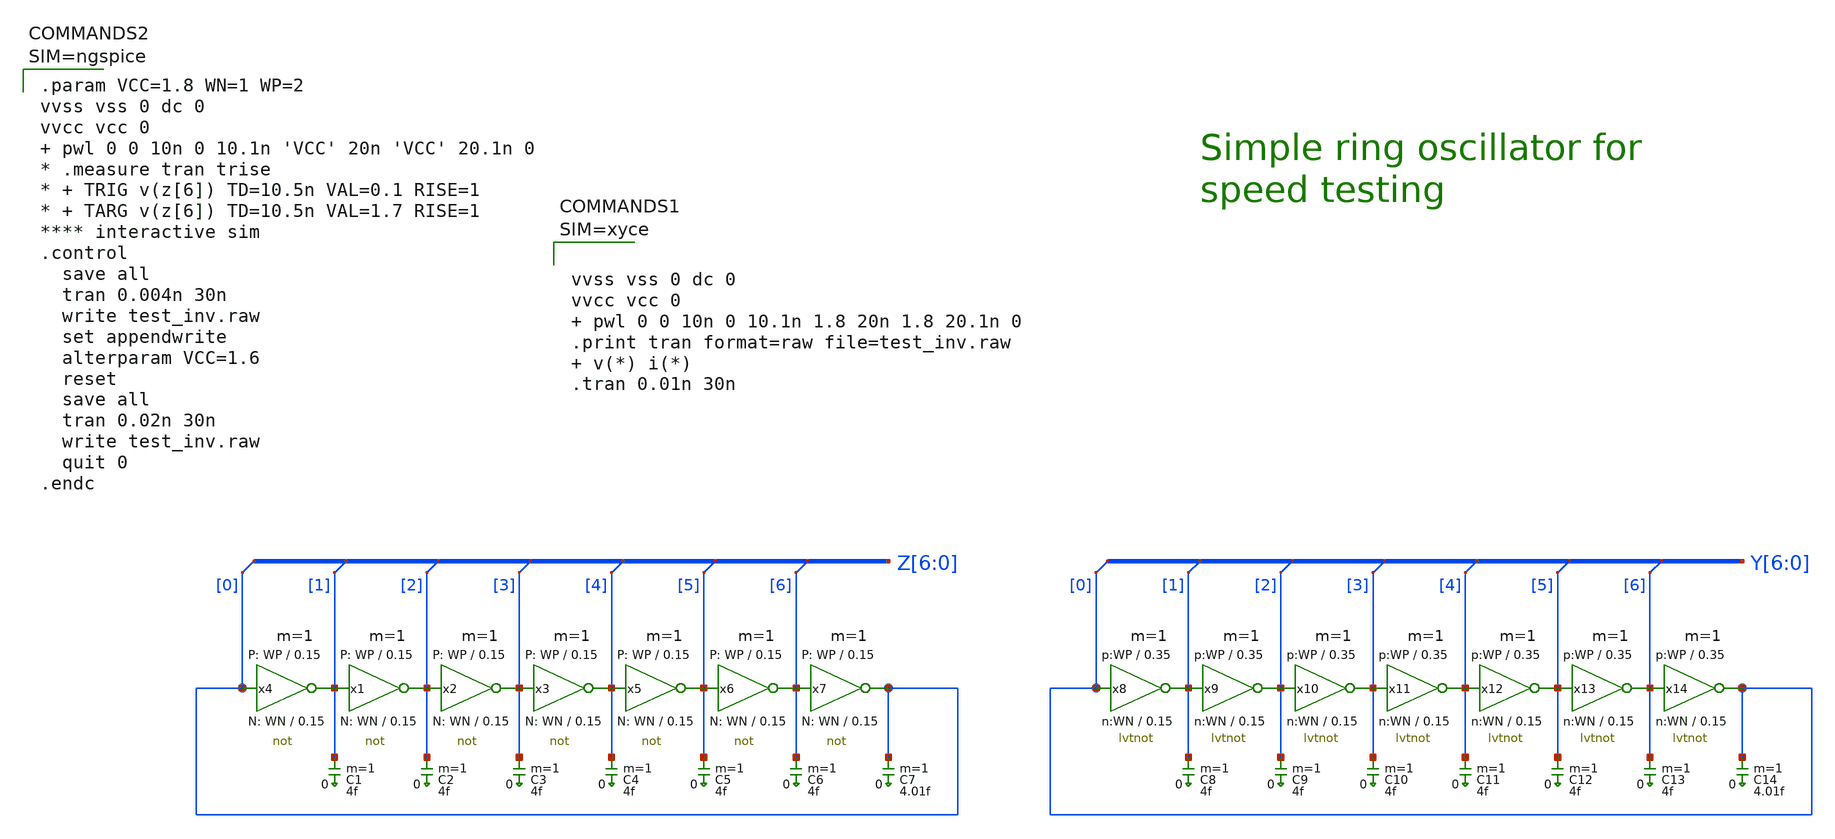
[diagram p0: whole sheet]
** sch_path: sky130A/xschem_libs/sky130_tests/test_inv/schematic/test_inv.sch
* Copyright 2021 Stefan Frederik Schippers
* Licensed under the Apache License, Version 2.0 (the "License");
* you may not use this file except in compliance with the License.
* You may obtain a copy of the License at
* https://www.apache.org/licenses/LICENSE-2.0
* Unless required by applicable law or agreed to in writing, software
* distributed under the License is distributed on an "AS IS" BASIS,
* WITHOUT WARRANTIES OR CONDITIONS OF ANY KIND, either express or implied.
* See the License for the specific language governing permissions and
* limitations under the License.
* StefanSchippers/xschem_sky130/sky130_tests/lvtnot.sch:
* Copyright 2020 Stefan Frederik Schippers
**.subckt test_inv
C1 Z[1] 0 4f m=1
C2 Z[2] 0 4f m=1
C3 Z[3] 0 4f m=1
C4 Z[4] 0 4f m=1
C5 Z[5] 0 4f m=1
C6 Z[6] 0 4f m=1
C7 Z[0] 0 4.01f m=1
C8 Y[1] 0 4f m=1
C9 Y[2] 0 4f m=1
C10 Y[3] 0 4f m=1
C11 Y[4] 0 4f m=1
C12 Y[5] 0 4f m=1
C13 Y[6] 0 4f m=1
C14 Y[0] 0 4.01f m=1
x4 Z[1] Z[0] VCC VSS not W_N=WN L_N=0.15 W_P=WP L_P=0.15 m=1
x1 Z[2] Z[1] VCC VSS not W_N=WN L_N=0.15 W_P=WP L_P=0.15 m=1
x2 Z[3] Z[2] VCC VSS not W_N=WN L_N=0.15 W_P=WP L_P=0.15 m=1
x3 Z[4] Z[3] VCC VSS not W_N=WN L_N=0.15 W_P=WP L_P=0.15 m=1
x5 Z[5] Z[4] VCC VSS not W_N=WN L_N=0.15 W_P=WP L_P=0.15 m=1
x6 Z[6] Z[5] VCC VSS not W_N=WN L_N=0.15 W_P=WP L_P=0.15 m=1
x7 Z[0] Z[6] VCC VSS not W_N=WN L_N=0.15 W_P=WP L_P=0.15 m=1
x8 Y[0] Y[1] VCC VSS lvtnot W_N=WN L_N=0.15 W_P=WP L_P=0.35 m=1
x9 Y[1] Y[2] VCC VSS lvtnot W_N=WN L_N=0.15 W_P=WP L_P=0.35 m=1
x10 Y[2] Y[3] VCC VSS lvtnot W_N=WN L_N=0.15 W_P=WP L_P=0.35 m=1
x11 Y[3] Y[4] VCC VSS lvtnot W_N=WN L_N=0.15 W_P=WP L_P=0.35 m=1
x12 Y[4] Y[5] VCC VSS lvtnot W_N=WN L_N=0.15 W_P=WP L_P=0.35 m=1
x13 Y[5] Y[6] VCC VSS lvtnot W_N=WN L_N=0.15 W_P=WP L_P=0.35 m=1
x14 Y[6] Y[0] VCC VSS lvtnot W_N=WN L_N=0.15 W_P=WP L_P=0.35 m=1
* tap: Z[6:0] --> Z[0]
* tap: Z[6:0] --> Z[1]
* tap: Z[6:0] --> Z[2]
* tap: Z[6:0] --> Z[3]
* tap: Z[6:0] --> Z[4]
* tap: Z[6:0] --> Z[5]
* tap: Z[6:0] --> Z[6]
* tap: Y[6:0] --> Y[0]
* tap: Y[6:0] --> Y[1]
* tap: Y[6:0] --> Y[2]
* tap: Y[6:0] --> Y[3]
* tap: Y[6:0] --> Y[4]
* tap: Y[6:0] --> Y[5]
* tap: Y[6:0] --> Y[6]
**** begin user architecture code


.param VCC=1.8 WN=1 WP=2
vvss vss 0 dc 0
vvcc vcc 0   pwl 0 0 10n 0 10.1n 'VCC' 20n 'VCC' 20.1n 0
* .measure tran trise
* + TRIG v(z[6]) TD=10.5n VAL=0.1 RISE=1
* + TARG v(z[6]) TD=10.5n VAL=1.7 RISE=1
**** interactive sim
.control
  save all
  tran 0.004n 30n
  write test_inv.raw
  set appendwrite
  alterparam VCC=1.6
  reset
  save all
  tran 0.02n 30n
  write test_inv.raw
  quit 0
.endc







** opencircuitdesign pdks install
.lib $::SKYWATER_MODELS/sky130.lib.spice tt

**** end user architecture code
**.ends

* expanding   symbol:  sky130_tests/not.sym # of pins=2
** sym_path: sky130_tests/not.sym
** sch_path: sky130_tests/not.sch
.subckt not y a VCCPIN VSSPIN     W_N=1 L_N=0.15 W_P=2 L_P=0.15
*.opin y
*.ipin a
XM1 DN a VSSPIN VSSPIN sky130_fd_pr__nfet_01v8 L=L_N W=W_N nf=1 ad='int((1 + 1)/2) * W_N / 1 * 0.29'
+ as='int((1 + 2)/2) * W_N / 1 * 0.29' pd='2*int((1 + 1)/2) * (W_N / 1 + 0.29)' ps='2*int((1 + 2)/2) * (W_N / 1 + 0.29)'
+ nrd='0.29 / W_N ' nrs='0.29 / W_N ' sa=0 sb=0 sd=0 mult=1 m=1
XM2 DP a VCCPIN VCCPIN sky130_fd_pr__pfet_01v8 L=L_P W=W_P nf=1 ad='int((nf+1)/2) * W/nf * 0.29' as='int((nf+2)/2) * W/nf * 0.29'
+ pd='2*int((nf+1)/2) * (W/nf + 0.29)' ps='2*int((nf+2)/2) * (W/nf + 0.29)' nrd='0.29 / W' nrs='0.29 / W'
+ sa=0 sb=0 sd=0 mult=1 m=1
Vmeas DP y 0
.save i(vmeas)
Vmeas1 y DN 0
.save i(vmeas1)
.save v(dp)
.save v(dn)
.ends


* expanding   symbol:  sky130_tests/lvtnot.sym # of pins=2
** sym_path: sky130_tests/lvtnot.sym
** sch_path: sky130_tests/lvtnot.sch
.subckt lvtnot a y VCCPIN VSSPIN     W_N=1 L_N=0.15 W_P=2 L_P=0.35
*.opin y
*.ipin a
XM1 y a VSSPIN VSSPIN sky130_fd_pr__nfet_01v8_lvt L=L_N W=W_N nf=1 ad='int((1 + 1)/2) * W_N / 1 * 0.29'
+ as='int((1 + 2)/2) * W_N / 1 * 0.29' pd='2*int((1 + 1)/2) * (W_N / 1 + 0.29)' ps='2*int((1 + 2)/2) * (W_N / 1 + 0.29)'
+ nrd='0.29 / W_N ' nrs='0.29 / W_N ' sa=0 sb=0 sd=0 mult=1 m=1
XM2 y a VCCPIN VCCPIN sky130_fd_pr__pfet_01v8_lvt L=L_P W=W_P nf=1 ad='int((1 + 1)/2) * W_P / 1 * 0.29'
+ as='int((1 + 2)/2) * W_P / 1 * 0.29' pd='2*int((1 + 1)/2) * (W_P / 1 + 0.29)' ps='2*int((1 + 2)/2) * (W_P / 1 + 0.29)'
+ nrd='0.29 / W_P ' nrs='0.29 / W_P ' sa=0 sb=0 sd=0 mult=1 m=1
.ends

.end
